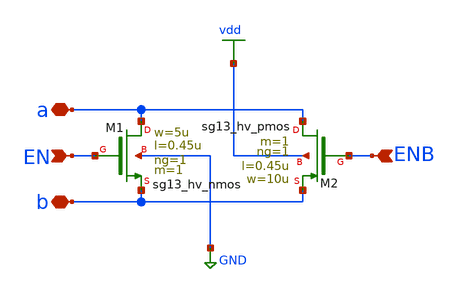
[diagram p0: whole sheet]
** sch_path: 3_real_circuits/tg_hv.sch
**.subckt tg_hv ENB EN b a
*.ipin ENB
*.ipin EN
*.iopin b
*.iopin a
XM2 a ENB b vdd sg13_hv_pmos w=10u l=0.45u ng=1 m=1 mm_ok=1
XM1 a EN b GND sg13_hv_nmos w=5u l=0.45u ng=1 m=1 mm_ok=1
**.ends
.GLOBAL vdd
.GLOBAL GND
.end
